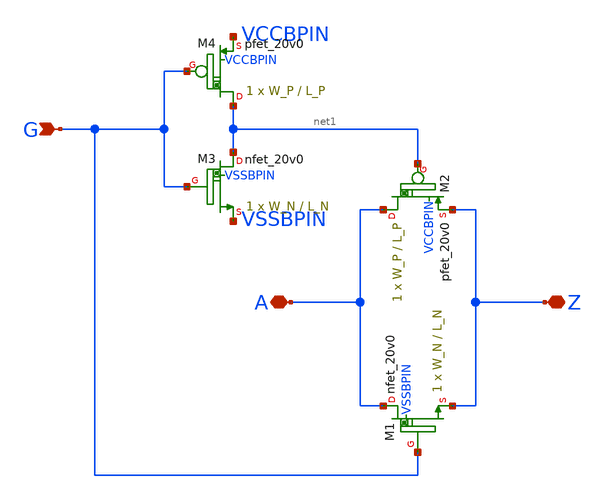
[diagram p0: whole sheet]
** sch_path: passgate_hv.sch
* Copyright 2021 Stefan Frederik Schippers
* Licensed under the Apache License, Version 2.0 (the "License");
* you may not use this file except in compliance with the License.
* You may obtain a copy of the License at
* https://www.apache.org/licenses/LICENSE-2.0
* Unless required by applicable law or agreed to in writing, software
* distributed under the License is distributed on an "AS IS" BASIS,
* WITHOUT WARRANTIES OR CONDITIONS OF ANY KIND, either express or implied.
* See the License for the specific language governing permissions and
* limitations under the License.
**.subckt passgate_hv A Z G
*.iopin A
*.iopin Z
*.ipin G
XM2 A net1 Z VCCBPIN sky130_fd_pr__pfet_20v0 L=L_P W=W_P m=1
XM1 A G Z VSSBPIN sky130_fd_pr__nfet_20v0 L=L_N W=W_N m=1
XM3 net1 G VSSBPIN VSSBPIN sky130_fd_pr__nfet_20v0 L=L_N W=W_N m=1
XM4 net1 G VCCBPIN VCCBPIN sky130_fd_pr__pfet_20v0 L=L_P W=W_P m=1
**.ends
.end
